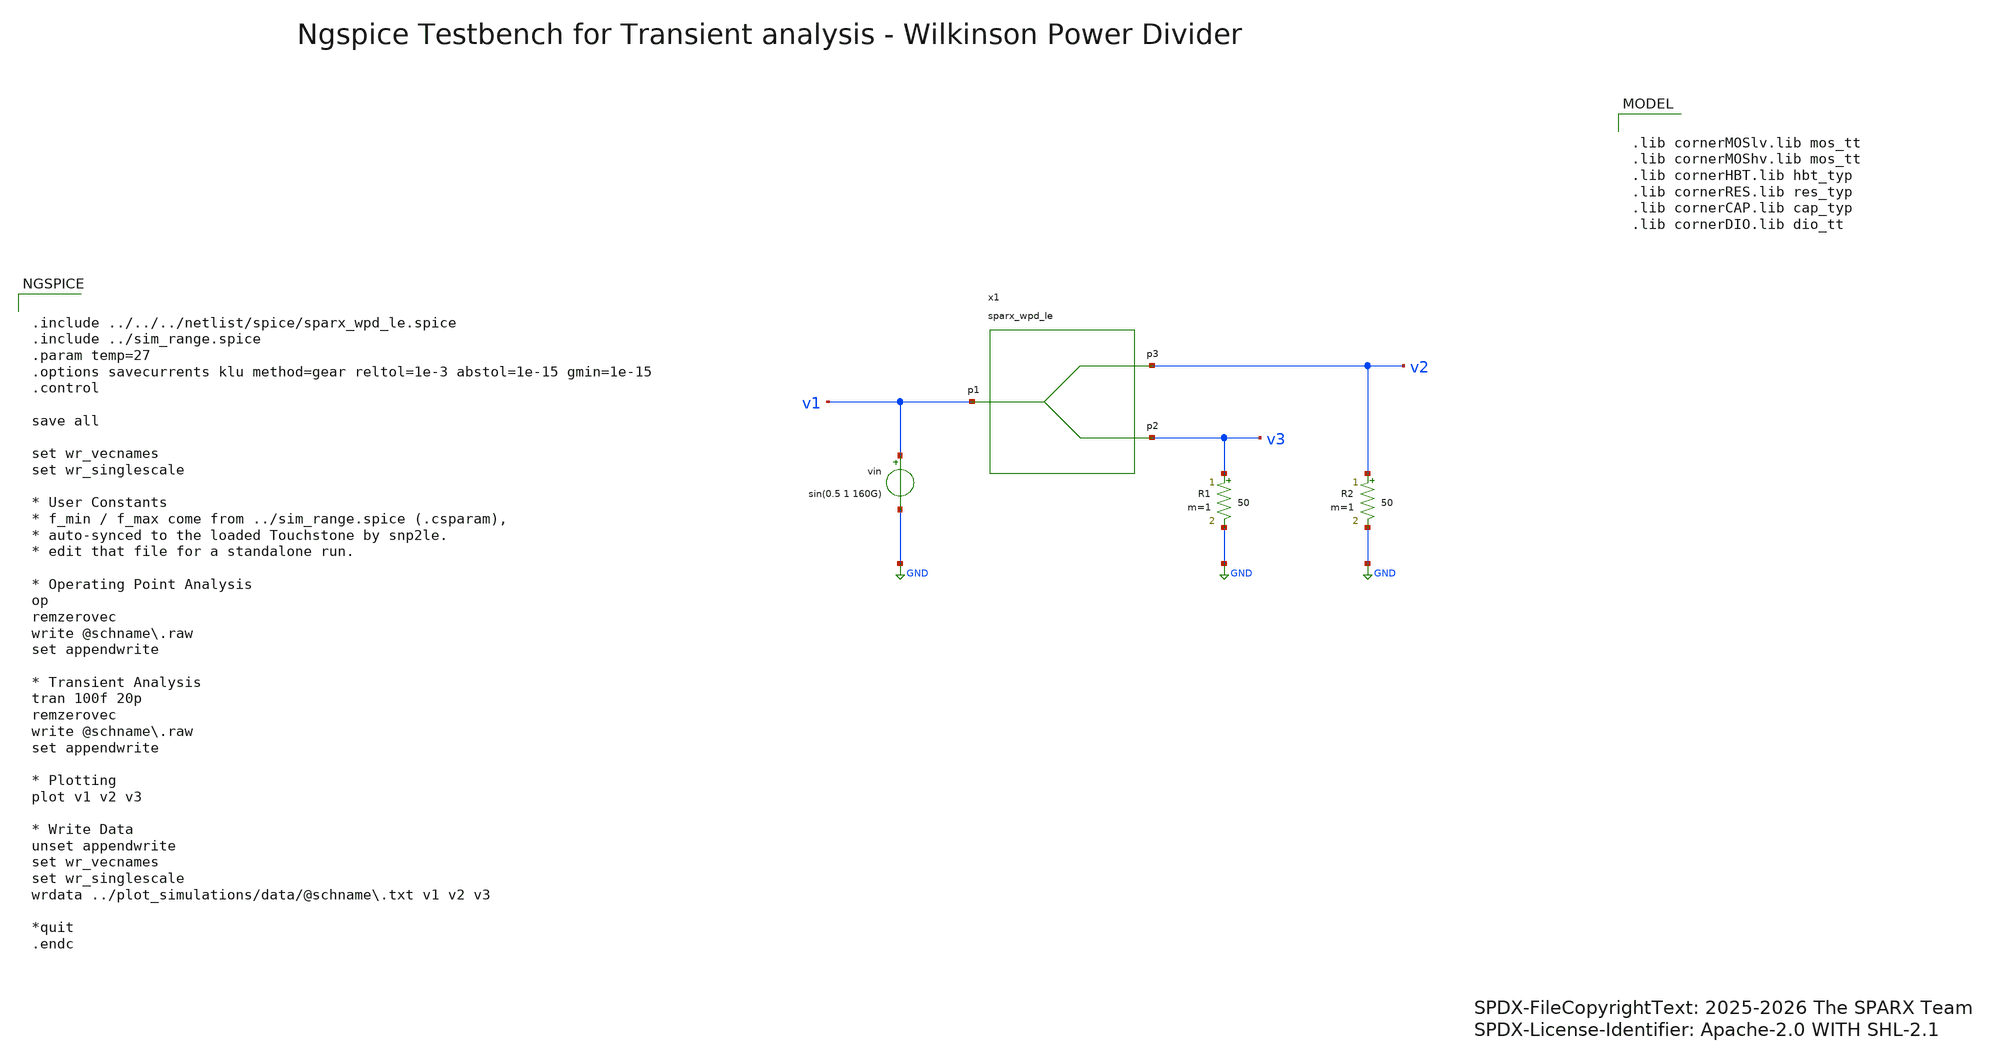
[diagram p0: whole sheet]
** sch_path: testbenches/xschem/sparx_wpd_le_tb_tran_ngspice.sch
* SPDX-FileCopyrightText: 2025-2026 The SPARX Team
* SPDX-License-Identifier: Apache-2.0 WITH SHL-2.1
**.subckt sparx_wpd_le_tb_tran_ngspice
x1 v1 v3 v2 sparx_wpd_le
R1 v3 GND 50 m=1
R2 v2 GND 50 m=1
vin v1 GND sin(0.5 1 160G)
**** begin user architecture code


.include ../../../netlist/spice/sparx_wpd_le.spice
.include ../sim_range.spice
.param temp=27
.options savecurrents klu method=gear reltol=1e-3 abstol=1e-15 gmin=1e-15
.control

save all

set wr_vecnames
set wr_singlescale

* User Constants
* f_min / f_max come from ../sim_range.spice (.csparam),
* auto-synced to the loaded Touchstone by snp2le.
* edit that file for a standalone run.

* Operating Point Analysis
op
remzerovec
write @schname\.raw
set appendwrite

* Transient Analysis
tran 100f 20p
remzerovec
write @schname\.raw
set appendwrite

* Plotting
plot v1 v2 v3

* Write Data
unset appendwrite
set wr_vecnames
set wr_singlescale
wrdata ../plot_simulations/data/@schname\.txt v1 v2 v3

*quit
.endc



.lib cornerMOSlv.lib mos_tt
.lib cornerMOShv.lib mos_tt
.lib cornerHBT.lib hbt_typ
.lib cornerRES.lib res_typ
.lib cornerCAP.lib cap_typ
.lib cornerDIO.lib dio_tt

**** end user architecture code
**.ends
.GLOBAL GND
.end
